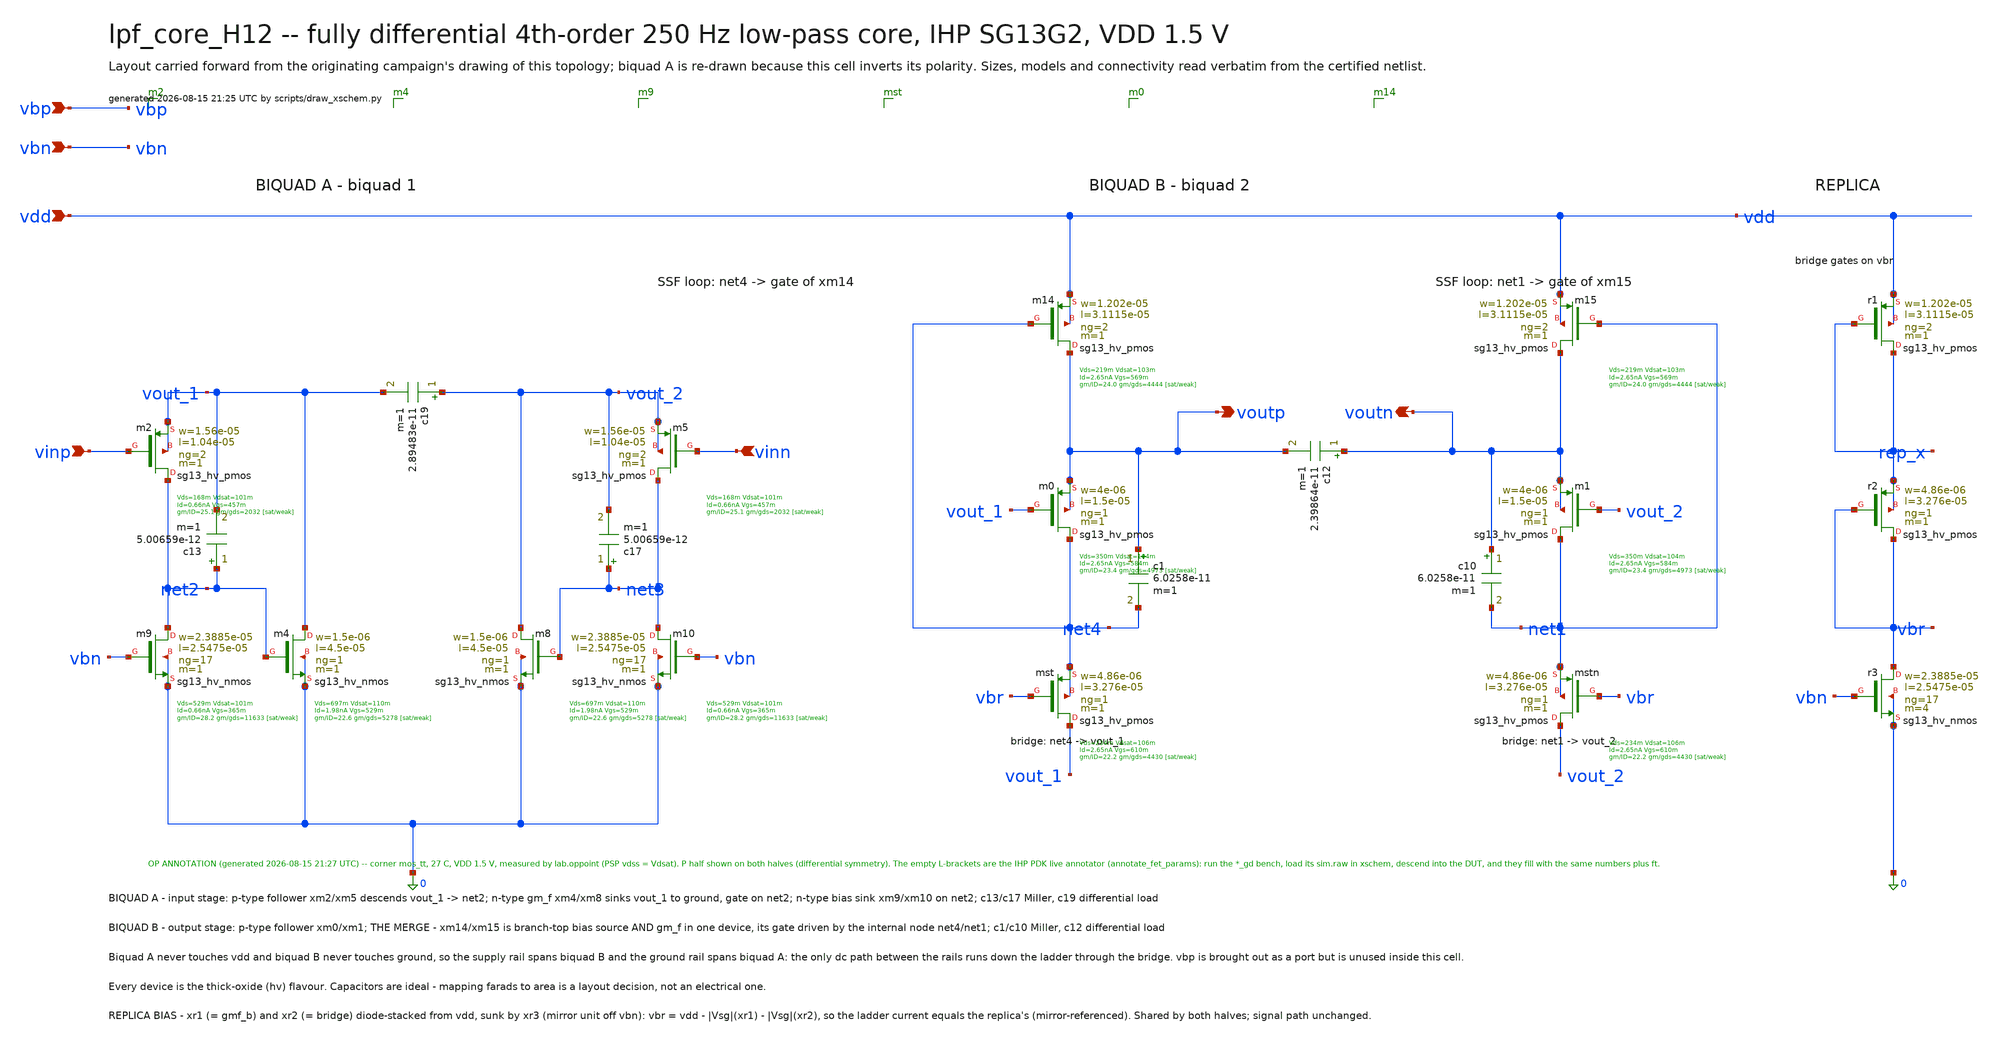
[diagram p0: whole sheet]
** sch_path: signoff/post-pvt/H12-robust/lpf_core_H12.sch
**.subckt lpf_core_H12 vinp vinn voutp voutn vdd vbn vbp
*.ipin vinp
*.ipin vinn
*.opin voutp
*.opin voutn
*.ipin vdd
*.ipin vbn
*.ipin vbp
Xm2 net2 vinp vout_1 vout_1 sg13_hv_pmos w=1.56e-05 l=1.04e-05 ng=2 m=1 mm_ok=1
Xm5 net3 vinn vout_2 vout_2 sg13_hv_pmos w=1.56e-05 l=1.04e-05 ng=2 m=1 mm_ok=1
Xm4 vout_1 net2 0 0 sg13_hv_nmos w=1.5e-06 l=4.5e-05 ng=1 m=1 mm_ok=1
Xm8 vout_2 net3 0 0 sg13_hv_nmos w=1.5e-06 l=4.5e-05 ng=1 m=1 mm_ok=1
Xm9 net2 vbn 0 0 sg13_hv_nmos w=2.3885e-05 l=2.5475e-05 ng=17 m=1 mm_ok=1
Xm10 net3 vbn 0 0 sg13_hv_nmos w=2.3885e-05 l=2.5475e-05 ng=17 m=1 mm_ok=1
Xmst vout_1 vbr net4 net4 sg13_hv_pmos w=4.86e-06 l=3.276e-05 ng=1 m=1 mm_ok=1
Xmstn vout_2 vbr net1 net1 sg13_hv_pmos w=4.86e-06 l=3.276e-05 ng=1 m=1 mm_ok=1
Xm0 net4 vout_1 voutp voutp sg13_hv_pmos w=4e-06 l=1.5e-05 ng=1 m=1 mm_ok=1
Xm1 net1 vout_2 voutn voutn sg13_hv_pmos w=4e-06 l=1.5e-05 ng=1 m=1 mm_ok=1
Xm14 voutp net4 vdd vdd sg13_hv_pmos w=1.202e-05 l=3.1115e-05 ng=2 m=1 mm_ok=1
Xm15 voutn net1 vdd vdd sg13_hv_pmos w=1.202e-05 l=3.1115e-05 ng=2 m=1 mm_ok=1
Xr1 rep_x rep_x vdd vdd sg13_hv_pmos w=1.202e-05 l=3.1115e-05 ng=2 m=1 mm_ok=1
Xr2 vbr vbr rep_x rep_x sg13_hv_pmos w=4.86e-06 l=3.276e-05 ng=1 m=1 mm_ok=1
Xr3 vbr vbn 0 0 sg13_hv_nmos w=2.3885e-05 l=2.5475e-05 ng=17 m=4 mm_ok=1
c13 net2 vout_1 5.00659e-12 m=1
c17 net3 vout_2 5.00659e-12 m=1
c19 vout_2 vout_1 2.89483e-11 m=1
c1 voutp net4 6.0258e-11 m=1
c10 voutn net1 6.0258e-11 m=1
c12 voutn voutp 2.39864e-11 m=1
**.ends
.end
